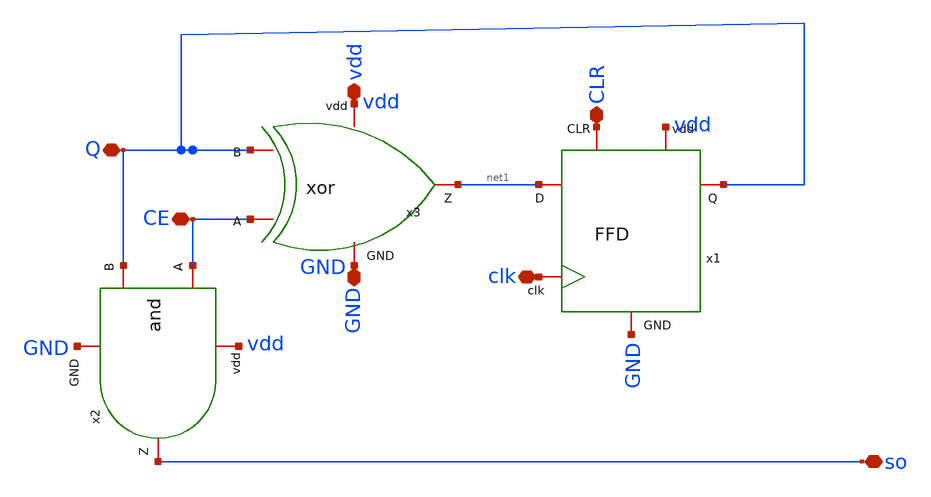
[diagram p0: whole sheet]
** sch_path: simbolos y esquematicos/count1b.sch
**.subckt count1b Q CLR clk so CE GND vdd
*.iopin Q
*.iopin CLR
*.iopin clk
*.iopin so
*.iopin CE
*.iopin GND
*.iopin vdd
x1 vdd GND CLR Q net1 clk FFD
x2 vdd CE so Q GND and
x3 vdd CE Q net1 GND xor
**.ends
.end
